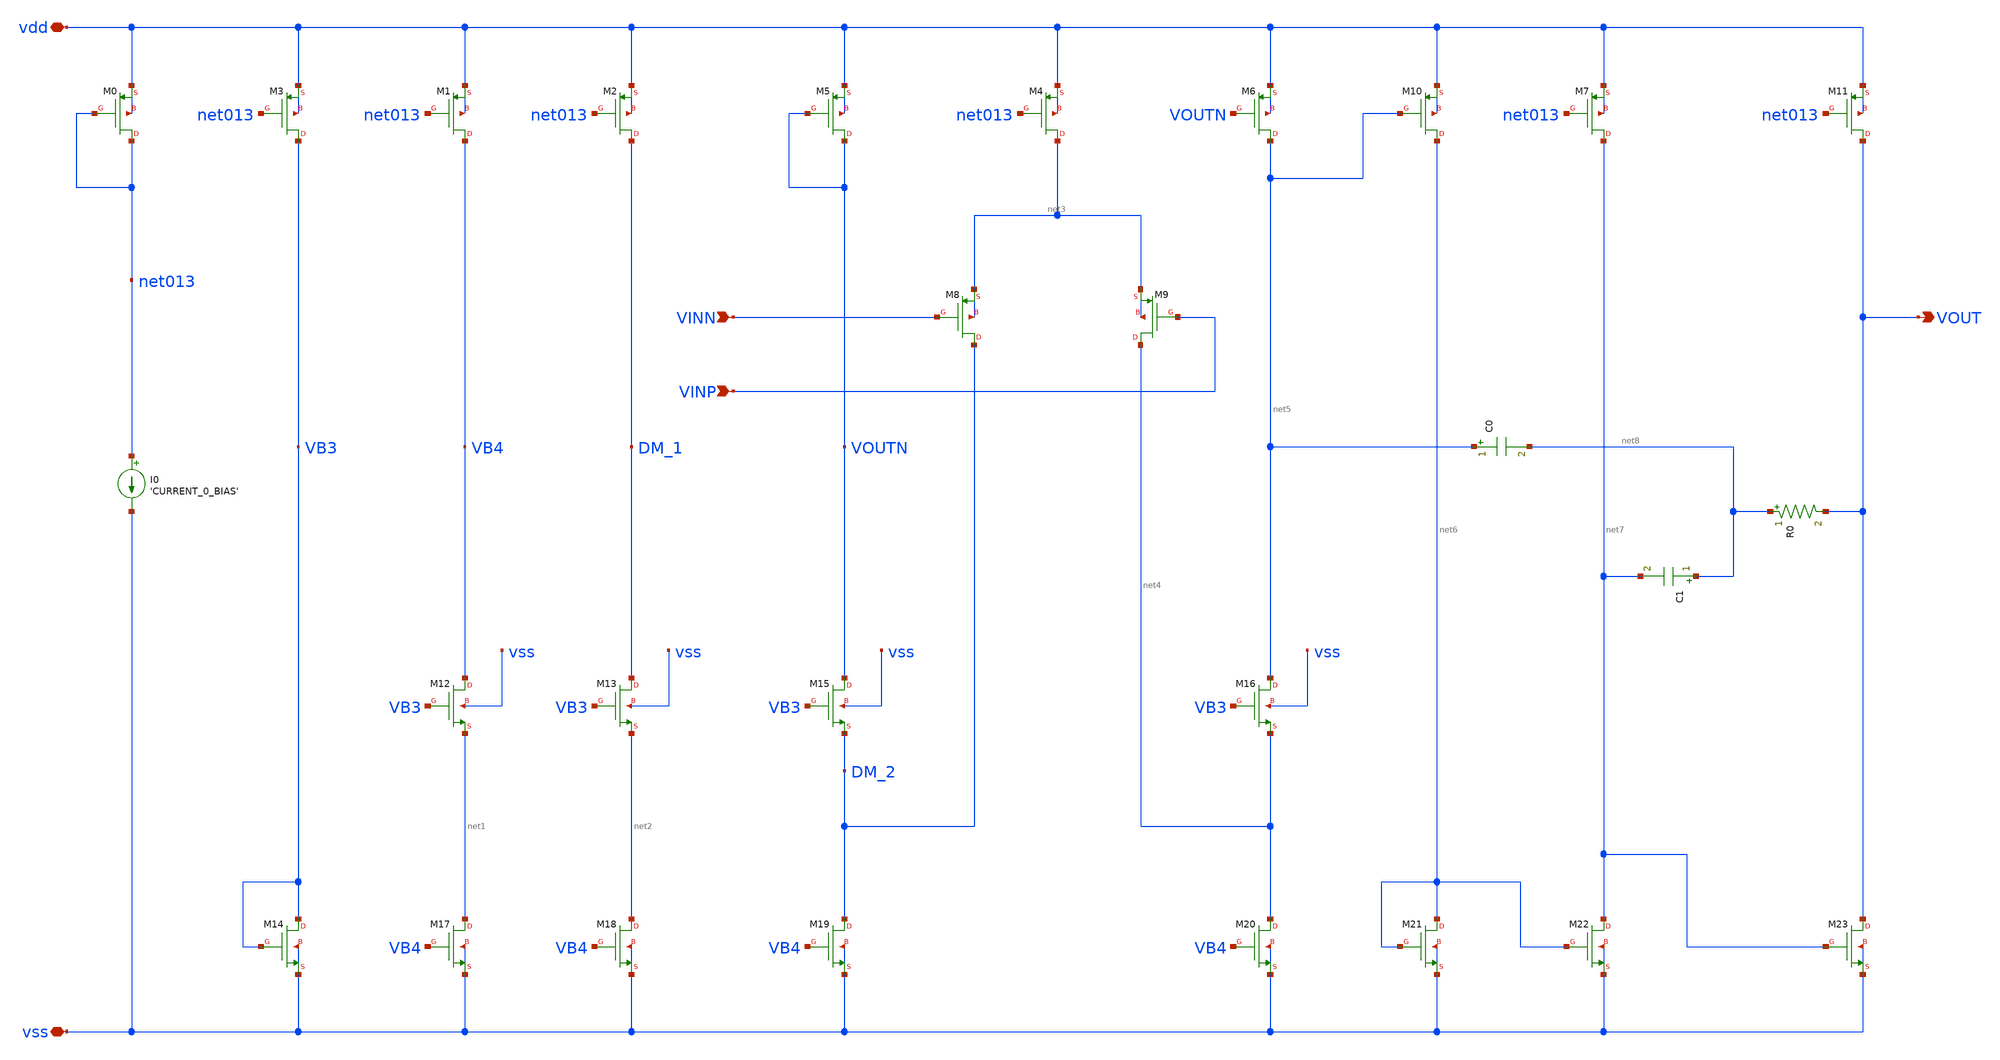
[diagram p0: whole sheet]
** sch_path: analog-db/drawings/publication/amp_009_leung_nmcnr.sch
**.subckt amp_009_leung_nmcnr VINN VINP VOUT vdd vss
*.ipin VINN
*.ipin VINP
*.opin VOUT
*.iopin vdd
*.iopin vss
XM0 net013 net013 vdd vdd sg13_lv_pmos w=x_dut_xm0_w l=x_dut_xm0_l ng=1 m=x_dut_xm0_m
I0 net013 vss 'CURRENT_0_BIAS'
XM3 VB3 net013 vdd vdd sg13_lv_pmos w=x_dut_xm3_w l=x_dut_xm3_l ng=1 m=x_dut_xm3_m
XM14 VB3 VB3 vss vss sg13_lv_nmos w=x_dut_xm14_w l=x_dut_xm14_l ng=1 m=x_dut_xm14_m
XM1 VB4 net013 vdd vdd sg13_lv_pmos w=x_dut_xm1_w l=x_dut_xm1_l ng=1 m=x_dut_xm1_m
XM12 VB4 VB3 net1 vss sg13_lv_nmos w=x_dut_xm12_w l=x_dut_xm12_l ng=1 m=x_dut_xm12_m
XM17 net1 VB4 vss vss sg13_lv_nmos w=x_dut_xm17_w l=x_dut_xm17_l ng=1 m=x_dut_xm17_m
XM2 DM_1 net013 vdd vdd sg13_lv_pmos w=x_dut_xm2_w l=x_dut_xm2_l ng=1 m=x_dut_xm2_m
XM13 DM_1 VB3 net2 vss sg13_lv_nmos w=x_dut_xm13_w l=x_dut_xm13_l ng=1 m=x_dut_xm13_m
XM18 net2 VB4 vss vss sg13_lv_nmos w=x_dut_xm18_w l=x_dut_xm18_l ng=1 m=x_dut_xm18_m
XM5 VOUTN VOUTN vdd vdd sg13_lv_pmos w=x_dut_xm5_w l=x_dut_xm5_l ng=1 m=x_dut_xm5_m
XM15 VOUTN VB3 DM_2 vss sg13_lv_nmos w=x_dut_xm15_w l=x_dut_xm15_l ng=1 m=x_dut_xm15_m
XM19 DM_2 VB4 vss vss sg13_lv_nmos w=x_dut_xm19_w l=x_dut_xm19_l ng=1 m=x_dut_xm19_m
XM8 DM_2 VINN net3 net3 sg13_lv_pmos w=x_dut_xm8_w l=x_dut_xm8_l ng=1 m=x_dut_xm8_m
XM9 net4 VINP net3 net3 sg13_lv_pmos w=x_dut_xm9_w l=x_dut_xm9_l ng=1 m=x_dut_xm9_m
XM4 net3 net013 vdd vdd sg13_lv_pmos w=x_dut_xm4_w l=x_dut_xm4_l ng=1 m=x_dut_xm4_m
XM6 net5 VOUTN vdd vdd sg13_lv_pmos w=x_dut_xm6_w l=x_dut_xm6_l ng=1 m=x_dut_xm6_m
XM16 net5 VB3 net4 vss sg13_lv_nmos w=x_dut_xm16_w l=x_dut_xm16_l ng=1 m=x_dut_xm16_m
XM20 net4 VB4 vss vss sg13_lv_nmos w=x_dut_xm20_w l=x_dut_xm20_l ng=1 m=x_dut_xm20_m
XM10 net6 net5 vdd vdd sg13_lv_pmos w=x_dut_xm10_w l=x_dut_xm10_l ng=1 m=x_dut_xm10_m
XM21 net6 net6 vss vss sg13_lv_nmos w=x_dut_xm21_w l=x_dut_xm21_l ng=1 m=x_dut_xm21_m
XM7 net7 net013 vdd vdd sg13_lv_pmos w=x_dut_xm7_w l=x_dut_xm7_l ng=1 m=x_dut_xm7_m
XM22 net7 net6 vss vss sg13_lv_nmos w=x_dut_xm22_w l=x_dut_xm22_l ng=1 m=x_dut_xm22_m
XM11 VOUT net013 vdd vdd sg13_lv_pmos w=x_dut_xm11_w l=x_dut_xm11_l ng=1 m=x_dut_xm11_m
XM23 VOUT net7 vss vss sg13_lv_nmos w=x_dut_xm23_w l=x_dut_xm23_l ng=1 m=x_dut_xm23_m
C0 net5 net8 'CAPACITOR_0' m=1
C1 net8 net7 'CAPACITOR_1' m=1
R0 net8 VOUT 'RESISTOR_0' m=1
**.ends
.end
